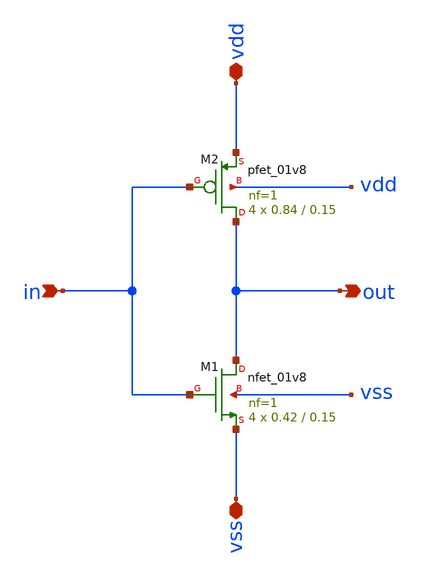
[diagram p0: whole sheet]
** sch_path: xschem/inverter_min_x4.sch
**.subckt inverter_min_x4 vss in out vdd
*.iopin vss
*.ipin in
*.opin out
*.iopin vdd
XM2 out in vdd vdd sky130_fd_pr__pfet_01v8 L=0.15 W=0.84 nf=1 ad='int((nf+1)/2) * W/nf * 0.29' as='int((nf+2)/2) * W/nf * 0.29'
+ pd='2*int((nf+1)/2) * (W/nf + 0.29)' ps='2*int((nf+2)/2) * (W/nf + 0.29)' nrd='0.29 / W' nrs='0.29 / W'
+ sa=0 sb=0 sd=0 mult=4 m=4
XM1 out in vss vss sky130_fd_pr__nfet_01v8 L=0.15 W=0.42 nf=1 ad='int((nf+1)/2) * W/nf * 0.29' as='int((nf+2)/2) * W/nf * 0.29'
+ pd='2*int((nf+1)/2) * (W/nf + 0.29)' ps='2*int((nf+2)/2) * (W/nf + 0.29)' nrd='0.29 / W' nrs='0.29 / W'
+ sa=0 sb=0 sd=0 mult=4 m=4
**.ends
.end
